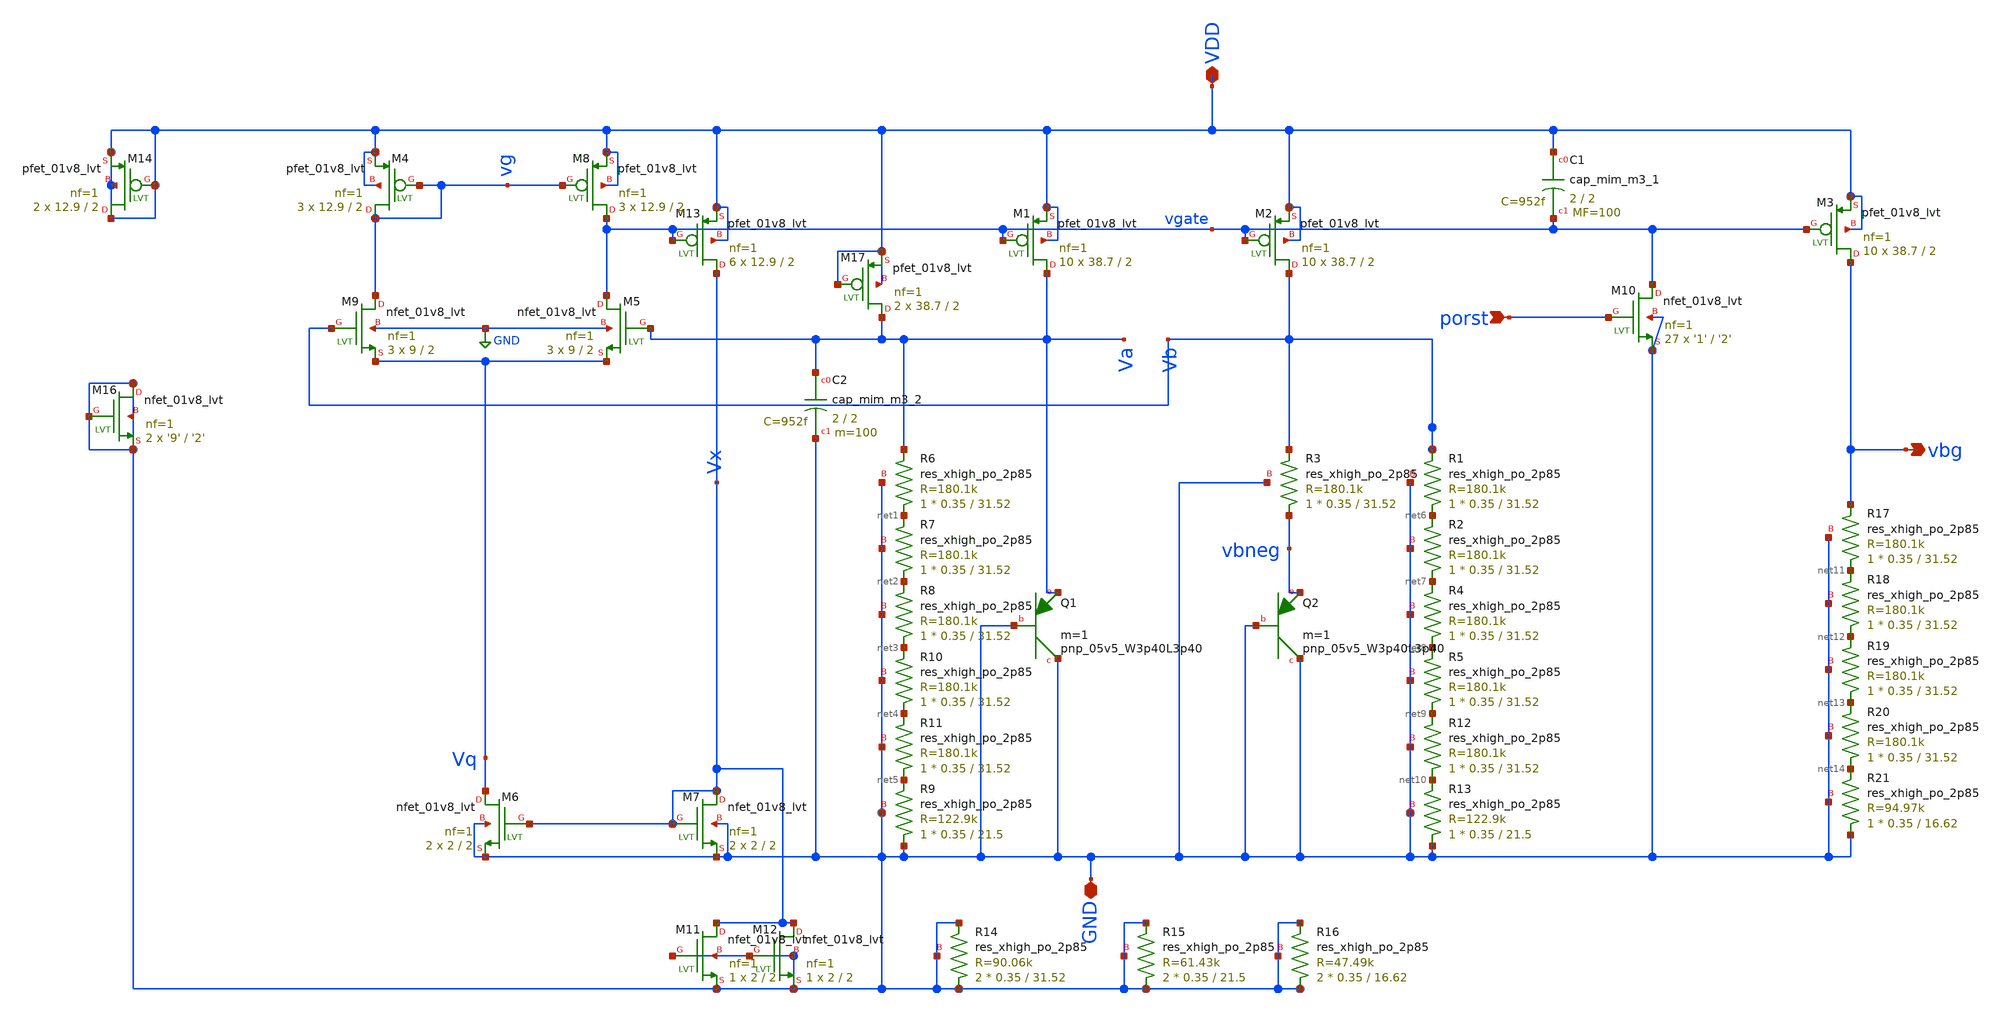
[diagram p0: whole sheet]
** sch_path: xschem/xschem/tsmc_bandgap_real_lvs.sch
**.subckt tsmc_bandgap_real_lvs porst vbg GND VDD
*.ipin porst
*.opin vbg
*.iopin GND
*.iopin VDD
XM5 vgate Va Vq GND sky130_fd_pr__nfet_01v8_lvt L=2 W=9 nf=1 ad='int((nf+1)/2) * W/nf * 0.29' as='int((nf+2)/2) * W/nf * 0.29'
+ pd='2*int((nf+1)/2) * (W/nf + 0.29)' ps='2*int((nf+2)/2) * (W/nf + 0.29)' nrd='0.29 / W' nrs='0.29 / W'
+ sa=0 sb=0 sd=0 mult=3 m=3
XM6 Vq Vx GND GND sky130_fd_pr__nfet_01v8_lvt L=2 W=2 nf=1 ad='int((nf+1)/2) * W/nf * 0.29' as='int((nf+2)/2) * W/nf * 0.29'
+ pd='2*int((nf+1)/2) * (W/nf + 0.29)' ps='2*int((nf+2)/2) * (W/nf + 0.29)' nrd='0.29 / W' nrs='0.29 / W'
+ sa=0 sb=0 sd=0 mult=2 m=2
XM9 vg Vb Vq GND sky130_fd_pr__nfet_01v8_lvt L=2 W=9 nf=1 ad='int((nf+1)/2) * W/nf * 0.29' as='int((nf+2)/2) * W/nf * 0.29'
+ pd='2*int((nf+1)/2) * (W/nf + 0.29)' ps='2*int((nf+2)/2) * (W/nf + 0.29)' nrd='0.29 / W' nrs='0.29 / W'
+ sa=0 sb=0 sd=0 mult=3 m=3
XM7 Vx Vx GND GND sky130_fd_pr__nfet_01v8_lvt L=2 W=2 nf=1 ad='int((nf+1)/2) * W/nf * 0.29' as='int((nf+2)/2) * W/nf * 0.29'
+ pd='2*int((nf+1)/2) * (W/nf + 0.29)' ps='2*int((nf+2)/2) * (W/nf + 0.29)' nrd='0.29 / W' nrs='0.29 / W'
+ sa=0 sb=0 sd=0 mult=2 m=2
XM13 Vx vgate VDD VDD sky130_fd_pr__pfet_01v8_lvt L=2 W=12.9 nf=1 ad='int((nf+1)/2) * W/nf * 0.29' as='int((nf+2)/2) * W/nf * 0.29'
+ pd='2*int((nf+1)/2) * (W/nf + 0.29)' ps='2*int((nf+2)/2) * (W/nf + 0.29)' nrd='0.29 / W' nrs='0.29 / W'
+ sa=0 sb=0 sd=0 mult=6 m=6
XM1 Va vgate VDD VDD sky130_fd_pr__pfet_01v8_lvt L=2 W=38.7 nf=1 ad='int((nf+1)/2) * W/nf * 0.29' as='int((nf+2)/2) * W/nf * 0.29'
+ pd='2*int((nf+1)/2) * (W/nf + 0.29)' ps='2*int((nf+2)/2) * (W/nf + 0.29)' nrd='0.29 / W' nrs='0.29 / W'
+ sa=0 sb=0 sd=0 mult=10 m=10
XM2 Vb vgate VDD VDD sky130_fd_pr__pfet_01v8_lvt L=2 W=38.7 nf=1 ad='int((nf+1)/2) * W/nf * 0.29' as='int((nf+2)/2) * W/nf * 0.29'
+ pd='2*int((nf+1)/2) * (W/nf + 0.29)' ps='2*int((nf+2)/2) * (W/nf + 0.29)' nrd='0.29 / W' nrs='0.29 / W'
+ sa=0 sb=0 sd=0 mult=10 m=10
XM3 vbg vgate VDD VDD sky130_fd_pr__pfet_01v8_lvt L=2 W=38.7 nf=1 ad='int((nf+1)/2) * W/nf * 0.29' as='int((nf+2)/2) * W/nf * 0.29'
+ pd='2*int((nf+1)/2) * (W/nf + 0.29)' ps='2*int((nf+2)/2) * (W/nf + 0.29)' nrd='0.29 / W' nrs='0.29 / W'
+ sa=0 sb=0 sd=0 mult=10 m=10
XM4 vg vg VDD VDD sky130_fd_pr__pfet_01v8_lvt L=2 W=12.9 nf=1 ad='int((nf+1)/2) * W/nf * 0.29' as='int((nf+2)/2) * W/nf * 0.29'
+ pd='2*int((nf+1)/2) * (W/nf + 0.29)' ps='2*int((nf+2)/2) * (W/nf + 0.29)' nrd='0.29 / W' nrs='0.29 / W'
+ sa=0 sb=0 sd=0 mult=3 m=3
XM8 vgate vg VDD VDD sky130_fd_pr__pfet_01v8_lvt L=2 W=12.9 nf=1 ad='int((nf+1)/2) * W/nf * 0.29' as='int((nf+2)/2) * W/nf * 0.29'
+ pd='2*int((nf+1)/2) * (W/nf + 0.29)' ps='2*int((nf+2)/2) * (W/nf + 0.29)' nrd='0.29 / W' nrs='0.29 / W'
+ sa=0 sb=0 sd=0 mult=3 m=3
XM10 vgate porst GND GND sky130_fd_pr__nfet_01v8_lvt L='2' W='1' nf=1 ad='int((nf+1)/2) * W/nf * 0.29'
+ as='int((nf+2)/2) * W/nf * 0.29' pd='2*int((nf+1)/2) * (W/nf + 0.29)' ps='2*int((nf+2)/2) * (W/nf + 0.29)'
+ nrd='0.29 / W' nrs='0.29 / W' sa=0 sb=0 sd=0 mult=27 m=27
XR6 net1 Va GND sky130_fd_pr__res_xhigh_po_2p85 L=31.52 mult=1 m=1
XR7 net2 net1 GND sky130_fd_pr__res_xhigh_po_2p85 L=31.52 mult=1 m=1
XR8 net3 net2 GND sky130_fd_pr__res_xhigh_po_2p85 L=31.52 mult=1 m=1
XR10 net4 net3 GND sky130_fd_pr__res_xhigh_po_2p85 L=31.52 mult=1 m=1
XR11 net5 net4 GND sky130_fd_pr__res_xhigh_po_2p85 L=31.52 mult=1 m=1
XR9 GND net5 GND sky130_fd_pr__res_xhigh_po_2p85 L=21.5 mult=1 m=1
XR3 vbneg Vb GND sky130_fd_pr__res_xhigh_po_2p85 L=31.52 mult=1 m=1
XR1 net6 Vb GND sky130_fd_pr__res_xhigh_po_2p85 L=31.52 mult=1 m=1
XR2 net7 net6 GND sky130_fd_pr__res_xhigh_po_2p85 L=31.52 mult=1 m=1
XR4 net8 net7 GND sky130_fd_pr__res_xhigh_po_2p85 L=31.52 mult=1 m=1
XR5 net9 net8 GND sky130_fd_pr__res_xhigh_po_2p85 L=31.52 mult=1 m=1
XR12 net10 net9 GND sky130_fd_pr__res_xhigh_po_2p85 L=31.52 mult=1 m=1
XR13 GND net10 GND sky130_fd_pr__res_xhigh_po_2p85 L=21.5 mult=1 m=1
XR17 net11 vbg GND sky130_fd_pr__res_xhigh_po_2p85 L=31.52 mult=1 m=1
XR18 net12 net11 GND sky130_fd_pr__res_xhigh_po_2p85 L=31.52 mult=1 m=1
XR19 net13 net12 GND sky130_fd_pr__res_xhigh_po_2p85 L=31.52 mult=1 m=1
XR20 net14 net13 GND sky130_fd_pr__res_xhigh_po_2p85 L=31.52 mult=1 m=1
XR21 GND net14 GND sky130_fd_pr__res_xhigh_po_2p85 L=16.62 mult=1 m=1
XR14 GND GND GND sky130_fd_pr__res_xhigh_po_2p85 L=31.52 mult=2 m=2
XR15 GND GND GND sky130_fd_pr__res_xhigh_po_2p85 L=21.5 mult=2 m=2
XR16 GND GND GND sky130_fd_pr__res_xhigh_po_2p85 L=16.62 mult=2 m=2
XM11 Vx GND GND GND sky130_fd_pr__nfet_01v8_lvt L=2 W=2 nf=1 ad='int((nf+1)/2) * W/nf * 0.29' as='int((nf+2)/2) * W/nf * 0.29'
+ pd='2*int((nf+1)/2) * (W/nf + 0.29)' ps='2*int((nf+2)/2) * (W/nf + 0.29)' nrd='0.29 / W' nrs='0.29 / W'
+ sa=0 sb=0 sd=0 mult=1 m=1
XM12 Vx GND GND GND sky130_fd_pr__nfet_01v8_lvt L=2 W=2 nf=1 ad='int((nf+1)/2) * W/nf * 0.29' as='int((nf+2)/2) * W/nf * 0.29'
+ pd='2*int((nf+1)/2) * (W/nf + 0.29)' ps='2*int((nf+2)/2) * (W/nf + 0.29)' nrd='0.29 / W' nrs='0.29 / W'
+ sa=0 sb=0 sd=0 mult=1 m=1
XM14 VDD VDD VDD VDD sky130_fd_pr__pfet_01v8_lvt L=2 W=12.9 nf=1 ad='int((nf+1)/2) * W/nf * 0.29' as='int((nf+2)/2) * W/nf * 0.29'
+ pd='2*int((nf+1)/2) * (W/nf + 0.29)' ps='2*int((nf+2)/2) * (W/nf + 0.29)' nrd='0.29 / W' nrs='0.29 / W'
+ sa=0 sb=0 sd=0 mult=2 m=2
XM16 GND GND GND GND sky130_fd_pr__nfet_01v8_lvt L='2' W='9' nf=1 ad='int((nf+1)/2) * W/nf * 0.29' as='int((nf+2)/2) * W/nf * 0.29'
+ pd='2*int((nf+1)/2) * (W/nf + 0.29)' ps='2*int((nf+2)/2) * (W/nf + 0.29)' nrd='0.29 / W' nrs='0.29 / W'
+ sa=0 sb=0 sd=0 mult=2 m=2
XM17 Va VDD VDD VDD sky130_fd_pr__pfet_01v8_lvt L=2 W=38.7 nf=1 ad='int((nf+1)/2) * W/nf * 0.29' as='int((nf+2)/2) * W/nf * 0.29'
+ pd='2*int((nf+1)/2) * (W/nf + 0.29)' ps='2*int((nf+2)/2) * (W/nf + 0.29)' nrd='0.29 / W' nrs='0.29 / W'
+ sa=0 sb=0 sd=0 mult=2 m=2
XC1 VDD vgate sky130_fd_pr__cap_mim_m3_1 W=2 L=2 MF=100 m=100
XC2 Va GND sky130_fd_pr__cap_mim_m3_2 W=2 L=2 MF=100 m=100
XQ1 GND GND Va sky130_fd_pr__pnp_05v5_W3p40L3p40 m=1
39Q2 GND GND vbneg sky130_fd_pr__pnp_05v5_W3p40L3p40 m=1
**.ends
.GLOBAL GND
.end
